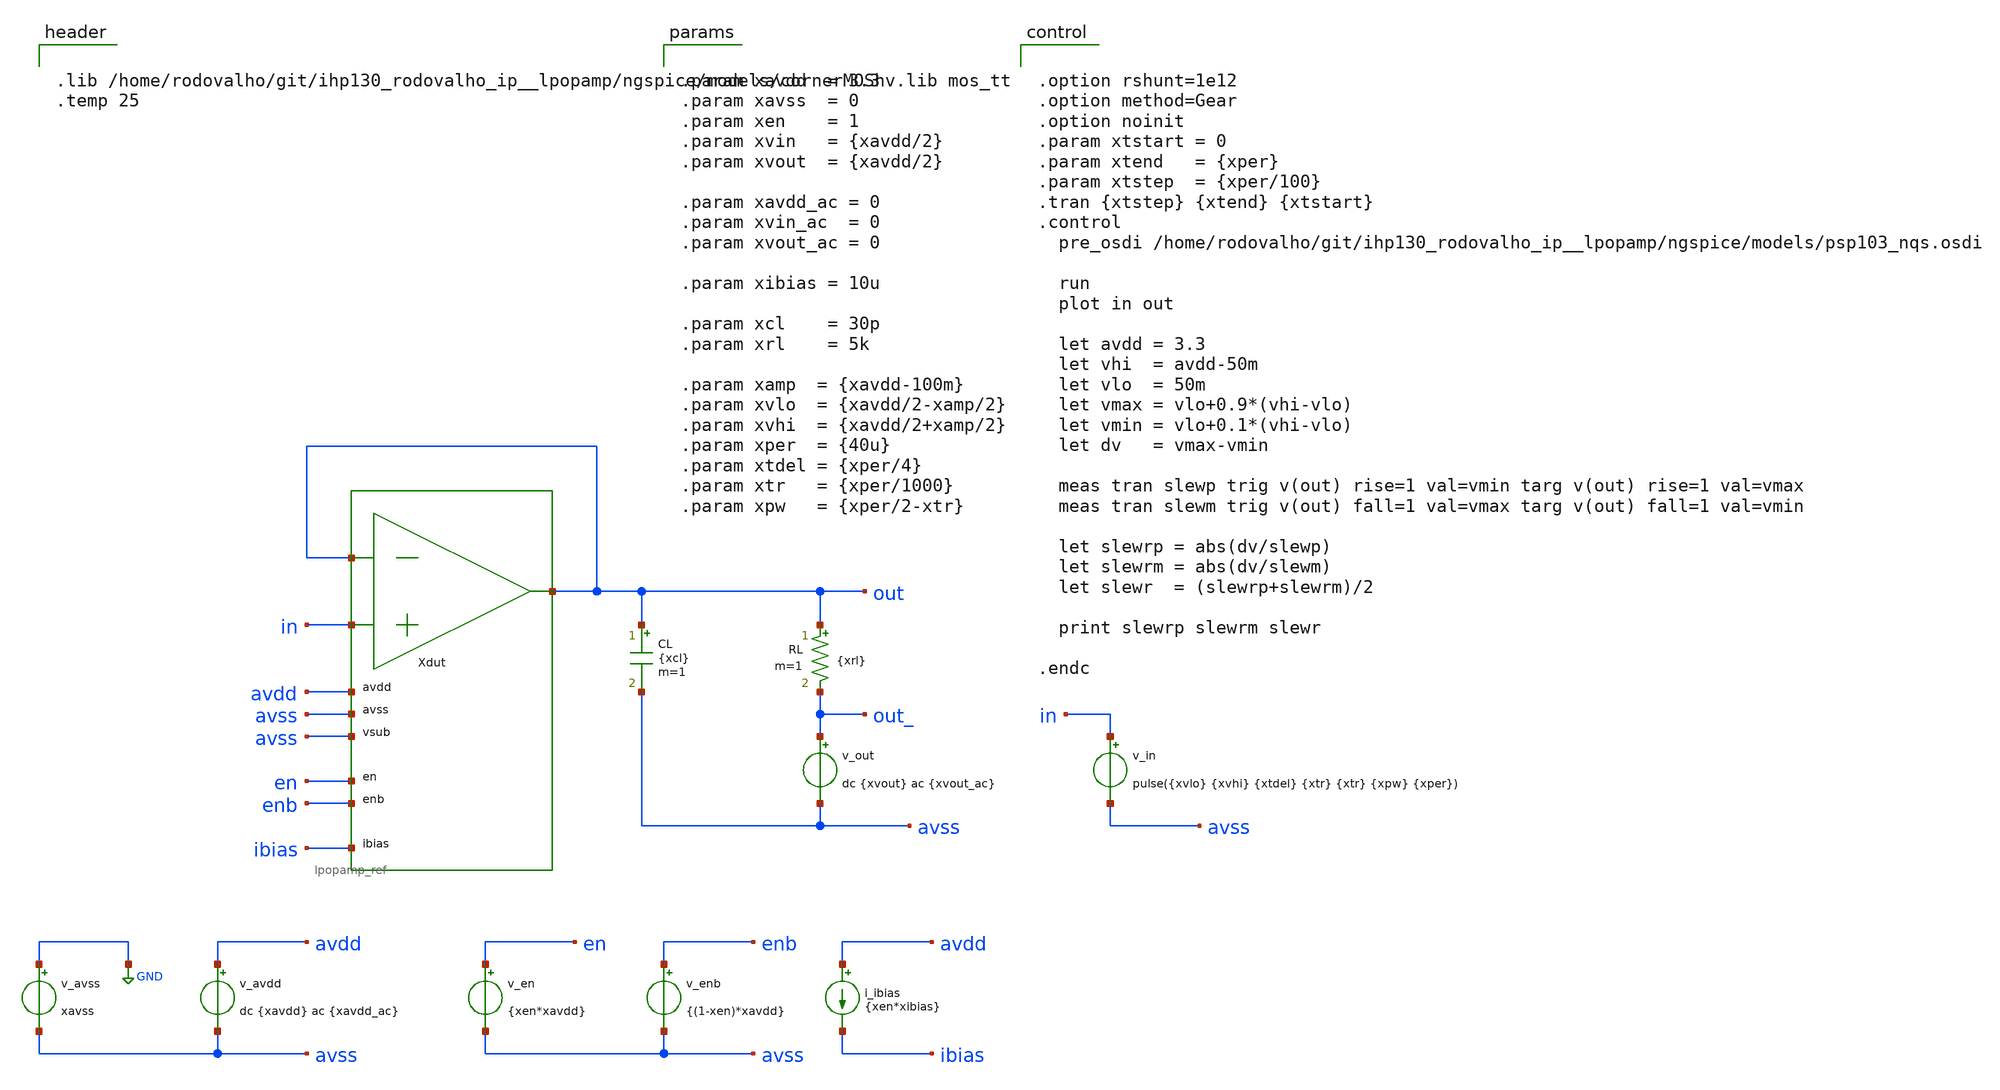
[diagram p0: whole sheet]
** sch_path: xschem/tb_lpopamp_buf_tran_step_large.sch
**.subckt tb_lpopamp_buf_tran_step_large
Xdut out in out avdd avss avss en enb ibias lpopamp_ref
v_avss GND avss xavss
v_avdd avdd avss dc {xavdd} ac {xavdd_ac}
v_in in avss pulse({xvlo} {xvhi} {xtdel} {xtr} {xtr} {xpw} {xper})
v_en en avss {xen*xavdd}
v_enb enb avss {(1-xen)*xavdd}
i_ibias avdd ibias {xen*xibias}
CL out avss {xcl} m=1
v_out out_ avss dc {xvout} ac {xvout_ac}
RL out out_ {xrl} m=1
**** begin user architecture code


.lib /home/rodovalho/git/ihp130_rodovalho_ip__lpopamp/ngspice/models/cornerMOShv.lib mos_tt
.temp 25




.option rshunt=1e12
.option method=Gear
.option noinit
.param xtstart = 0
.param xtend   = {xper}
.param xtstep  = {xper/100}
.tran {xtstep} {xtend} {xtstart}
.control
  pre_osdi /home/rodovalho/git/ihp130_rodovalho_ip__lpopamp/ngspice/models/psp103_nqs.osdi

  run
  plot in out

  let avdd = 3.3
  let vhi  = avdd-50m
  let vlo  = 50m
  let vmax = vlo+0.9*(vhi-vlo)
  let vmin = vlo+0.1*(vhi-vlo)
  let dv   = vmax-vmin

  meas tran slewp trig v(out) rise=1 val=vmin targ v(out) rise=1 val=vmax
  meas tran slewm trig v(out) fall=1 val=vmax targ v(out) fall=1 val=vmin

  let slewrp = abs(dv/slewp)
  let slewrm = abs(dv/slewm)
  let slewr  = (slewrp+slewrm)/2

  print slewrp slewrm slewr

.endc




.param xavdd  = 3.3
.param xavss  = 0
.param xen    = 1
.param xvin   = {xavdd/2}
.param xvout  = {xavdd/2}

.param xavdd_ac = 0
.param xvin_ac  = 0
.param xvout_ac = 0

.param xibias = 10u

.param xcl    = 30p
.param xrl    = 5k

.param xamp  = {xavdd-100m}
.param xvlo  = {xavdd/2-xamp/2}
.param xvhi  = {xavdd/2+xamp/2}
.param xper  = {40u}
.param xtdel = {xper/4}
.param xtr   = {xper/1000}
.param xpw   = {xper/2-xtr}


**** end user architecture code
**.ends
.GLOBAL GND
.end
